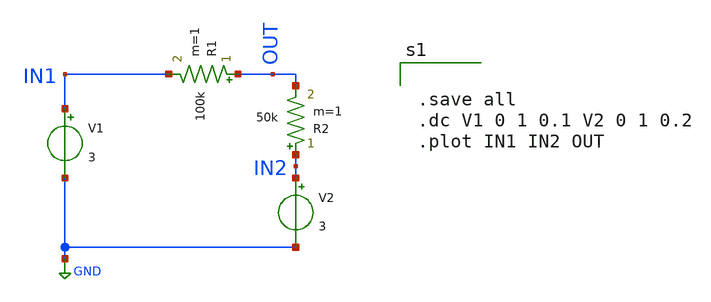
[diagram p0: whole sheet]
** sch_path: test_sch2.sch
**.subckt test_sch2
R1 OUT IN1 100k m=1
R2 IN2 OUT 50k m=1
V1 IN1 GND 3
V2 IN2 GND 3
**** begin user architecture code


.save all
.dc V1 0 1 0.1 V2 0 1 0.2
.plot IN1 IN2 OUT


**** end user architecture code
**.ends
.GLOBAL GND
.end
